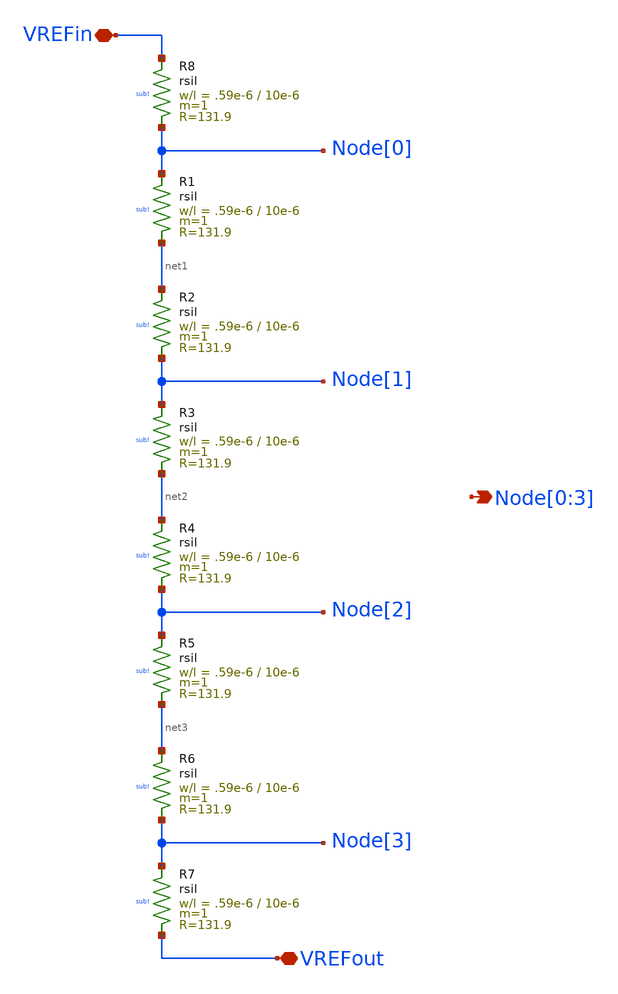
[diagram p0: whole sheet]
** sch_path: ihp130_cells/Resistor_String/ihp130_resistor_string.sch
**.subckt ihp130_resistor_string VREFout VREFin Node[0],Node[1],Node[2],Node[3]
*.iopin VREFout
*.iopin VREFin
*.opin Node[0],Node[1],Node[2],Node[3]
XR8 VREFin Node[0] sub! rsil w=.59e-6 l=10e-6 m=1 mm_ok=1
XR1 Node[0] net1 sub! rsil w=.59e-6 l=10e-6 m=1 mm_ok=1
XR2 net1 Node[1] sub! rsil w=.59e-6 l=10e-6 m=1 mm_ok=1
XR3 Node[1] net2 sub! rsil w=.59e-6 l=10e-6 m=1 mm_ok=1
XR4 net2 Node[2] sub! rsil w=.59e-6 l=10e-6 m=1 mm_ok=1
XR5 Node[2] net3 sub! rsil w=.59e-6 l=10e-6 m=1 mm_ok=1
XR6 net3 Node[3] sub! rsil w=.59e-6 l=10e-6 m=1 mm_ok=1
XR7 Node[3] VREFout sub! rsil w=.59e-6 l=10e-6 m=1 mm_ok=1
**.ends
.end
